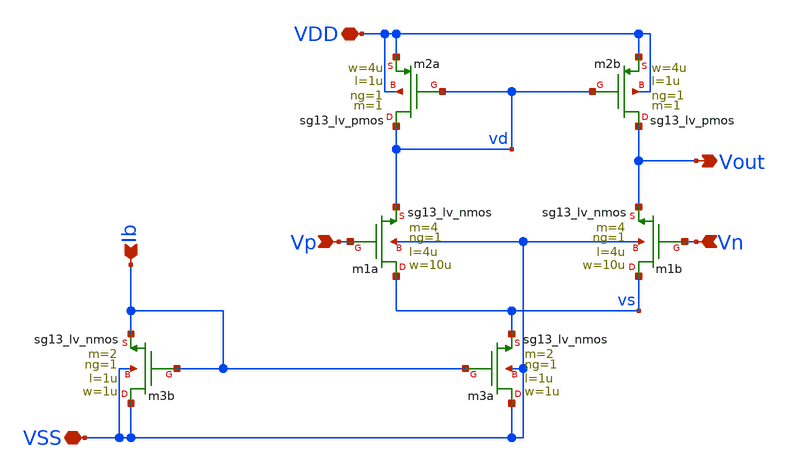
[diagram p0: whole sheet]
** sch_path: ota-5t.sch
**.subckt ota-5t VDD Vp Vout Vn VSS Ib
*.iopin VDD
*.ipin Vp
*.opin Vout
*.ipin Vn
*.iopin VSS
*.ipin Ib
Xm1a vs Vp vd VSS sg13_lv_nmos w=10u l=4u ng=1 m=4 mm_ok=1
Xm2b Vout vd VDD VDD sg13_lv_pmos w=4u l=1u ng=1 m=1 mm_ok=1
Xm2a vd vd VDD VDD sg13_lv_pmos w=4u l=1u ng=1 m=1 mm_ok=1
Xm3a VSS Ib vs VSS sg13_lv_nmos w=1u l=1u ng=1 m=2 mm_ok=1
Xm1b vs Vn Vout VSS sg13_lv_nmos w=10u l=4u ng=1 m=4 mm_ok=1
Xm3b VSS Ib Ib VSS sg13_lv_nmos w=1u l=1u ng=1 m=2 mm_ok=1
**.ends
.end
